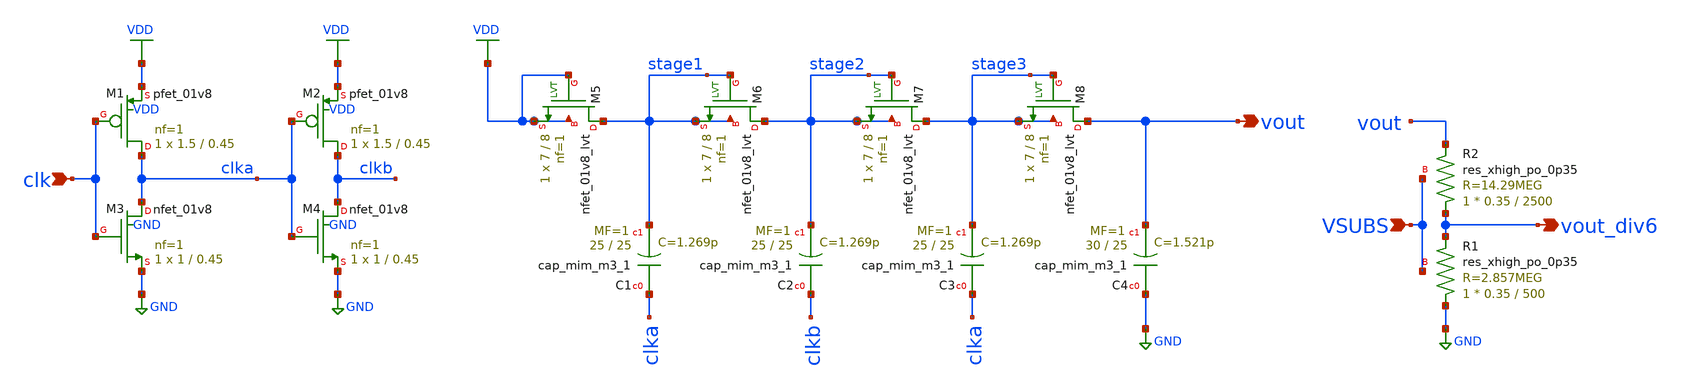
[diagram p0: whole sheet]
** sch_path: xschem/dickson.sch
**.subckt dickson clk vout vout_div6 VSUBS
*.ipin clk
*.opin vout
*.opin vout_div6
*.ipin VSUBS
XM1 clka clk VDD VDD sky130_fd_pr__pfet_01v8 L=0.45 W=1.5 nf=1 ad='int((nf+1)/2) * W/nf * 0.29' as='int((nf+2)/2) * W/nf * 0.29'
+ pd='2*int((nf+1)/2) * (W/nf + 0.29)' ps='2*int((nf+2)/2) * (W/nf + 0.29)' nrd='0.29 / W' nrs='0.29 / W'
+ sa=0 sb=0 sd=0 mult=1 m=1
XM3 clka clk GND GND sky130_fd_pr__nfet_01v8 L=0.45 W=1 nf=1 ad='int((nf+1)/2) * W/nf * 0.29' as='int((nf+2)/2) * W/nf * 0.29'
+ pd='2*int((nf+1)/2) * (W/nf + 0.29)' ps='2*int((nf+2)/2) * (W/nf + 0.29)' nrd='0.29 / W' nrs='0.29 / W'
+ sa=0 sb=0 sd=0 mult=1 m=1
XM2 clkb clka VDD VDD sky130_fd_pr__pfet_01v8 L=0.45 W=1.5 nf=1 ad='int((nf+1)/2) * W/nf * 0.29' as='int((nf+2)/2) * W/nf * 0.29'
+ pd='2*int((nf+1)/2) * (W/nf + 0.29)' ps='2*int((nf+2)/2) * (W/nf + 0.29)' nrd='0.29 / W' nrs='0.29 / W'
+ sa=0 sb=0 sd=0 mult=1 m=1
XM4 clkb clka GND GND sky130_fd_pr__nfet_01v8 L=0.45 W=1 nf=1 ad='int((nf+1)/2) * W/nf * 0.29' as='int((nf+2)/2) * W/nf * 0.29'
+ pd='2*int((nf+1)/2) * (W/nf + 0.29)' ps='2*int((nf+2)/2) * (W/nf + 0.29)' nrd='0.29 / W' nrs='0.29 / W'
+ sa=0 sb=0 sd=0 mult=1 m=1
XC3 clka stage3 sky130_fd_pr__cap_mim_m3_1 W=25 L=25 MF=1 m=1
XM5 stage1 VDD VDD VDD sky130_fd_pr__nfet_01v8_lvt L=8 W=7 nf=1 ad='int((nf+1)/2) * W/nf * 0.29' as='int((nf+2)/2) * W/nf * 0.29'
+ pd='2*int((nf+1)/2) * (W/nf + 0.29)' ps='2*int((nf+2)/2) * (W/nf + 0.29)' nrd='0.29 / W' nrs='0.29 / W'
+ sa=0 sb=0 sd=0 mult=1 m=1
XC1 clka stage1 sky130_fd_pr__cap_mim_m3_1 W=25 L=25 MF=1 m=1
XM6 stage2 stage1 stage1 stage1 sky130_fd_pr__nfet_01v8_lvt L=8 W=7 nf=1 ad='int((nf+1)/2) * W/nf * 0.29'
+ as='int((nf+2)/2) * W/nf * 0.29' pd='2*int((nf+1)/2) * (W/nf + 0.29)' ps='2*int((nf+2)/2) * (W/nf + 0.29)'
+ nrd='0.29 / W' nrs='0.29 / W' sa=0 sb=0 sd=0 mult=1 m=1
XM7 stage3 stage2 stage2 stage2 sky130_fd_pr__nfet_01v8_lvt L=8 W=7 nf=1 ad='int((nf+1)/2) * W/nf * 0.29'
+ as='int((nf+2)/2) * W/nf * 0.29' pd='2*int((nf+1)/2) * (W/nf + 0.29)' ps='2*int((nf+2)/2) * (W/nf + 0.29)'
+ nrd='0.29 / W' nrs='0.29 / W' sa=0 sb=0 sd=0 mult=1 m=1
XC2 clkb stage2 sky130_fd_pr__cap_mim_m3_1 W=25 L=25 MF=1 m=1
XM8 vout stage3 stage3 stage3 sky130_fd_pr__nfet_01v8_lvt L=8 W=7 nf=1 ad='int((nf+1)/2) * W/nf * 0.29'
+ as='int((nf+2)/2) * W/nf * 0.29' pd='2*int((nf+1)/2) * (W/nf + 0.29)' ps='2*int((nf+2)/2) * (W/nf + 0.29)'
+ nrd='0.29 / W' nrs='0.29 / W' sa=0 sb=0 sd=0 mult=1 m=1
XC4 GND vout sky130_fd_pr__cap_mim_m3_1 W=30 L=25 MF=1 m=1
XR2 vout_div6 vout VSUBS sky130_fd_pr__res_xhigh_po_0p35 L=2500 mult=1 m=1
XR1 GND vout_div6 VSUBS sky130_fd_pr__res_xhigh_po_0p35 L=500 mult=1 m=1
**.ends
.GLOBAL GND
.GLOBAL VDD
.end
